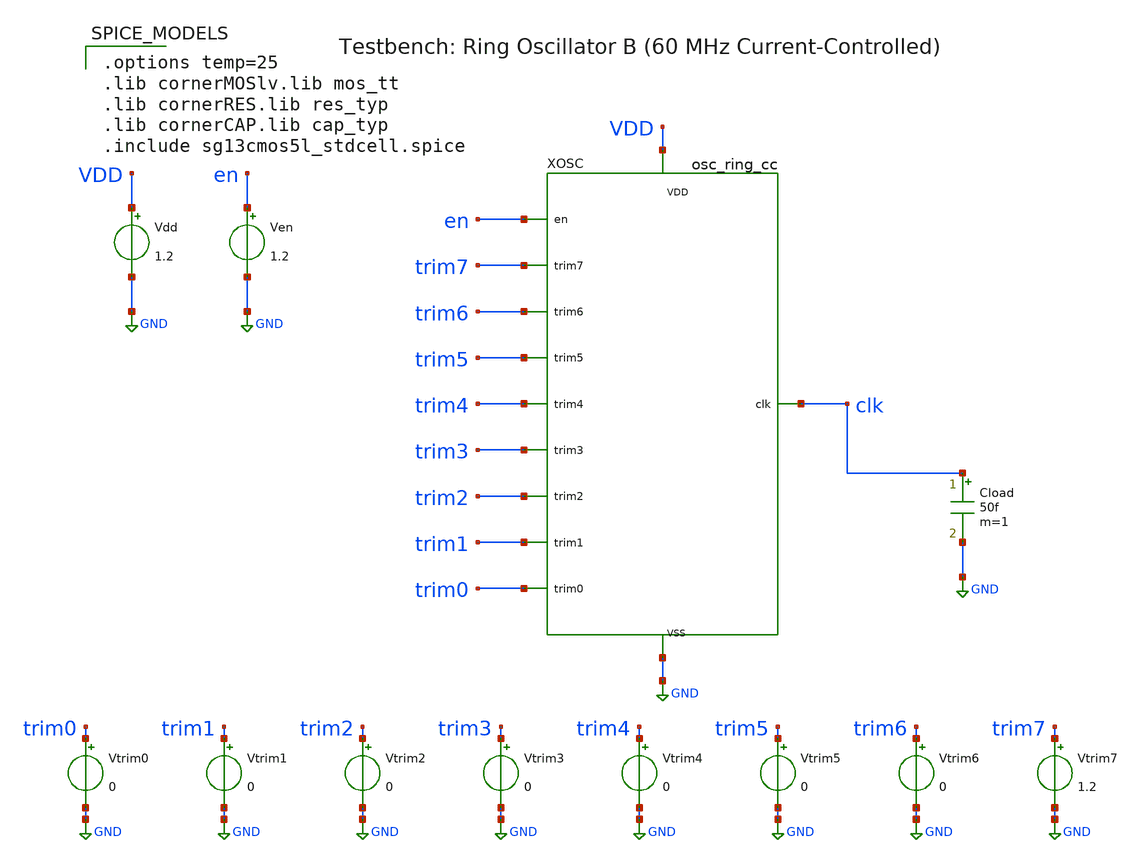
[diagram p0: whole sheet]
** sch_path: analog/osc_ring_cc/tb_osc_ring_cc.sch
**.subckt tb_osc_ring_cc
XOSC VDD GND en trim7 trim6 trim5 trim4 trim3 trim2 trim1 trim0 clk osc_ring_cc
Vdd VDD GND 1.2
Ven en GND 1.2
Vtrim0 trim0 GND 0
Vtrim1 trim1 GND 0
Vtrim2 trim2 GND 0
Vtrim3 trim3 GND 0
Vtrim4 trim4 GND 0
Vtrim5 trim5 GND 0
Vtrim6 trim6 GND 0
Vtrim7 trim7 GND 1.2
Cload clk GND 50f m=1
**** begin user architecture code

.options temp=25
.lib cornerMOSlv.lib mos_tt
.lib cornerRES.lib res_typ
.lib cornerCAP.lib cap_typ
.include sg13cmos5l_stdcell.spice


**** end user architecture code
**.ends

* expanding   symbol:  osc_ring_cc/osc_ring_cc.sym # of pins=12
** sym_path: analog/osc_ring_cc/osc_ring_cc.sym
** sch_path: analog/osc_ring_cc/osc_ring_cc.sch
.subckt osc_ring_cc VDD VSS en trim7 trim6 trim5 trim4 trim3 trim2 trim1 trim0 clk
*.iopin VDD
*.iopin VSS
*.ipin en
*.ipin trim7
*.ipin trim6
*.ipin trim5
*.ipin trim4
*.ipin trim3
*.ipin trim2
*.ipin trim1
*.ipin trim0
*.opin clk
XBIAS VDD VSS en net1 vnbias net2 bias
XIDAC VDD VSS en vnbias trim7 trim6 trim5 trim4 trim3 trim2 trim1 trim0 ictrl idac_8b
XCCO VDD VSS en ictrl clk cco_core
* noconn #net1
* noconn #net2
.ends


* expanding   symbol:  bias/bias.sym # of pins=6
** sym_path: analog/bias/bias.sym
** sch_path: analog/bias/bias.sch
.subckt bias VDD VSS en vpbias vnbias ibias_out
*.iopin VDD
*.iopin VSS
*.ipin en
*.opin vpbias
*.opin vnbias
*.opin ibias_out
XMEN_P enb en VDD VDD sg13_lv_pmos w=0.5u l=0.5u ng=1 m=1 mm_ok=1
XMEN_N enb en VSS VSS sg13_lv_nmos w=0.25u l=0.5u ng=1 m=1 mm_ok=1
XMSU_EN net1 enb VDD VDD sg13_lv_pmos w=0.3u l=1.0u ng=1 m=1 mm_ok=1
XMSU_P1 net2 VSS net1 VDD sg13_lv_pmos w=0.15u l=10u ng=1 m=1 mm_ok=1
XMSU_P2 net3 VSS net2 VDD sg13_lv_pmos w=0.15u l=10u ng=1 m=1 mm_ok=1
XMSU_N net3 vnbias VSS VSS sg13_lv_nmos w=4.0u l=0.5u ng=1 m=1 mm_ok=1
XMSU_INJ vpbias net3 VSS VSS sg13_lv_nmos w=0.5u l=1.0u ng=1 m=1 mm_ok=1
XMP1 vnbias vpbias VDD VDD sg13_lv_pmos w=1.0u l=4.0u ng=1 m=1 mm_ok=1
XMN1 vnbias vnbias VSS VSS sg13_lv_nmos w=0.3u l=4.0u ng=1 m=1 mm_ok=1
XMP2 vpbias vpbias VDD VDD sg13_lv_pmos w=1.0u l=4.0u ng=1 m=1 mm_ok=1
XMN2 vpbias vnbias net4 VSS sg13_lv_nmos w=0.3u l=4.0u ng=1 m=4 mm_ok=1
XR_BIAS net4 VSS VSS rppd w=0.5e-6 l=20.0e-6 m=1 b=19 mm_ok=1
XMP_OFF vpbias en VDD VDD sg13_lv_pmos w=1.0u l=0.5u ng=1 m=1 mm_ok=1
XMN_OFF vnbias enb VSS VSS sg13_lv_nmos w=1.0u l=0.5u ng=1 m=1 mm_ok=1
XMP_OUT ibias_out vpbias VDD VDD sg13_lv_pmos w=1.0u l=4.0u ng=1 m=1 mm_ok=1
.ends


* expanding   symbol:  osc_ring_cc/idac_8b.sym # of pins=13
** sym_path: analog/osc_ring_cc/idac_8b.sym
** sch_path: analog/osc_ring_cc/idac_8b.sch
.subckt idac_8b VDD VSS en vnbias trim7 trim6 trim5 trim4 trim3 trim2 trim1 trim0 ictrl
*.iopin VDD
*.iopin VSS
*.ipin en
*.ipin vnbias
*.ipin trim7
*.ipin trim6
*.ipin trim5
*.ipin trim4
*.ipin trim3
*.ipin trim2
*.ipin trim1
*.ipin trim0
*.opin ictrl
XMN_DIV vpdac vnbias VSS VSS sg13_lv_nmos w=0.3u l=4.0u ng=1 m=1 mm_ok=1
XMP_IN vpdac vpdac VDD VDD sg13_lv_pmos w=1.5u l=4.0u ng=1 m=2 mm_ok=1
XMP_DAC_OFF vpdac en VDD VDD sg13_lv_pmos w=0.5u l=0.5u ng=1 m=1 mm_ok=1
XINV_EN enb en VDD VSS sg13cmos5l_inv_1
XINV_B0 b0_b trim0 VDD VSS sg13cmos5l_inv_1
XINV_B1 b1_b trim1 VDD VSS sg13cmos5l_inv_1
XINV_B2 b2_b trim2 VDD VSS sg13cmos5l_inv_1
XINV_B3 b3_b trim3 VDD VSS sg13cmos5l_inv_1
XINV_B4 b4_b trim4 VDD VSS sg13cmos5l_inv_1
XINV_A t3_b trim7 VDD VSS sg13cmos5l_inv_1
XN_AB t5_b trim7 trim6 VDD VSS sg13cmos5l_nand2_2
XI_AB ab t5_b VDD VSS sg13cmos5l_inv_1
XN_ABC t6_b ab trim5 VDD VSS sg13cmos5l_nand2_2
XN_BC bc_n trim6 trim5 VDD VSS sg13cmos5l_nand2_2
XI_BC bc bc_n VDD VSS sg13cmos5l_inv_1
XNO_T2 t2_b trim7 bc VDD VSS sg13cmos5l_nor2_1
XNO_BORC borc_n trim6 trim5 VDD VSS sg13cmos5l_nor2_1
XI_BORC borc borc_n VDD VSS sg13cmos5l_inv_1
XN_T4 t4_b trim7 borc VDD VSS sg13cmos5l_nand2_2
XNO_T1 t1_b trim7 trim6 VDD VSS sg13cmos5l_nor2_1
XNO_T0 t0_b trim7 borc VDD VSS sg13cmos5l_nor2_1
XMPC_PED net1 vpdac VDD VDD sg13_lv_pmos w=0.5u l=4.0u ng=1 m=48 mm_ok=1
XMPS_PED ictrl enb net1 VDD sg13_lv_pmos w=1.0u l=0.2u ng=1 m=4 mm_ok=1
XMPC_B0 net2 vpdac VDD VDD sg13_lv_pmos w=0.5u l=4.0u ng=1 m=1 mm_ok=1
XMPS_B0 ictrl b0_b net2 VDD sg13_lv_pmos w=1.0u l=0.2u ng=1 m=1 mm_ok=1
XMPC_B1 net3 vpdac VDD VDD sg13_lv_pmos w=0.5u l=4.0u ng=1 m=2 mm_ok=1
XMPS_B1 ictrl b1_b net3 VDD sg13_lv_pmos w=1.0u l=0.2u ng=1 m=1 mm_ok=1
XMPC_B2 net4 vpdac VDD VDD sg13_lv_pmos w=0.5u l=4.0u ng=1 m=4 mm_ok=1
XMPS_B2 ictrl b2_b net4 VDD sg13_lv_pmos w=1.0u l=0.2u ng=1 m=1 mm_ok=1
XMPC_B3 net5 vpdac VDD VDD sg13_lv_pmos w=0.5u l=4.0u ng=1 m=8 mm_ok=1
XMPS_B3 ictrl b3_b net5 VDD sg13_lv_pmos w=1.0u l=0.2u ng=1 m=1 mm_ok=1
XMPC_B4 net6 vpdac VDD VDD sg13_lv_pmos w=0.5u l=4.0u ng=1 m=16 mm_ok=1
XMPS_B4 ictrl b4_b net6 VDD sg13_lv_pmos w=1.0u l=0.2u ng=1 m=2 mm_ok=1
XMPC_T0 net7 vpdac VDD VDD sg13_lv_pmos w=0.5u l=4.0u ng=1 m=32 mm_ok=1
XMPS_T0 ictrl t0_b net7 VDD sg13_lv_pmos w=1.0u l=0.2u ng=1 m=4 mm_ok=1
XMPC_T1 net8 vpdac VDD VDD sg13_lv_pmos w=0.5u l=4.0u ng=1 m=32 mm_ok=1
XMPS_T1 ictrl t1_b net8 VDD sg13_lv_pmos w=1.0u l=0.2u ng=1 m=4 mm_ok=1
XMPC_T2 net9 vpdac VDD VDD sg13_lv_pmos w=0.5u l=4.0u ng=1 m=32 mm_ok=1
XMPS_T2 ictrl t2_b net9 VDD sg13_lv_pmos w=1.0u l=0.2u ng=1 m=4 mm_ok=1
XMPC_T3 net10 vpdac VDD VDD sg13_lv_pmos w=0.5u l=4.0u ng=1 m=32 mm_ok=1
XMPS_T3 ictrl t3_b net10 VDD sg13_lv_pmos w=1.0u l=0.2u ng=1 m=4 mm_ok=1
XMPC_T4 net11 vpdac VDD VDD sg13_lv_pmos w=0.5u l=4.0u ng=1 m=32 mm_ok=1
XMPS_T4 ictrl t4_b net11 VDD sg13_lv_pmos w=1.0u l=0.2u ng=1 m=4 mm_ok=1
XMPC_T5 net12 vpdac VDD VDD sg13_lv_pmos w=0.5u l=4.0u ng=1 m=32 mm_ok=1
XMPS_T5 ictrl t5_b net12 VDD sg13_lv_pmos w=1.0u l=0.2u ng=1 m=4 mm_ok=1
XMPC_T6 net13 vpdac VDD VDD sg13_lv_pmos w=0.5u l=4.0u ng=1 m=32 mm_ok=1
XMPS_T6 ictrl t6_b net13 VDD sg13_lv_pmos w=1.0u l=0.2u ng=1 m=4 mm_ok=1
.ends


* expanding   symbol:  osc_ring_cc/cco_core.sym # of pins=5
** sym_path: analog/osc_ring_cc/cco_core.sym
** sch_path: analog/osc_ring_cc/cco_core.sch
.subckt cco_core VDD VSS en ictrl clk
*.iopin VDD
*.iopin VSS
*.ipin en
*.ipin ictrl
*.opin clk
XINV_EN enb en VDD VSS sg13cmos5l_inv_1
XMN_BIAS ictrl ictrl VSS VSS sg13_lv_nmos w=2.0u l=1.0u ng=1 m=2 mm_ok=1
XMP_BIAS vctrl_p vctrl_p VDD VDD sg13_lv_pmos w=4.0u l=1.0u ng=1 m=2 mm_ok=1
XMN_BMIR vctrl_p ictrl VSS VSS sg13_lv_nmos w=2.0u l=1.0u ng=1 m=2 mm_ok=1
XMP_POFF vctrl_p en VDD VDD sg13_lv_pmos w=0.5u l=0.5u ng=1 m=1 mm_ok=1
XMN_NOFF ictrl enb VSS VSS sg13_lv_nmos w=0.5u l=0.5u ng=1 m=1 mm_ok=1
XMPC_0 net1 vctrl_p VDD VDD sg13_lv_pmos w=4.0u l=1.0u ng=1 m=1 mm_ok=1
XMPI_0 n1 n0 net1 VDD sg13_lv_pmos w=1.0u l=0.2u ng=1 m=1 mm_ok=1
XMNI_0 n1 n0 net2 VSS sg13_lv_nmos w=0.5u l=0.2u ng=1 m=1 mm_ok=1
XMNC_0 net2 ictrl VSS VSS sg13_lv_nmos w=2.0u l=1.0u ng=1 m=1 mm_ok=1
XCC_0 n1 VSS cap_cmomf w=2.4e-6 l=2.4e-6 mmin=1 mmax=4 subblock=0 rfmodel=0 subscale=1 m=1 mm_ok=1
XMPC_1 net3 vctrl_p VDD VDD sg13_lv_pmos w=4.0u l=1.0u ng=1 m=1 mm_ok=1
XMPI_1 n2 n1 net3 VDD sg13_lv_pmos w=1.0u l=0.2u ng=1 m=1 mm_ok=1
XMNI_1 n2 n1 net4 VSS sg13_lv_nmos w=0.5u l=0.2u ng=1 m=1 mm_ok=1
XMNC_1 net4 ictrl VSS VSS sg13_lv_nmos w=2.0u l=1.0u ng=1 m=1 mm_ok=1
XCC_1 n2 VSS cap_cmomf w=2.4e-6 l=2.4e-6 mmin=1 mmax=4 subblock=0 rfmodel=0 subscale=1 m=1 mm_ok=1
XMPC_2 net5 vctrl_p VDD VDD sg13_lv_pmos w=4.0u l=1.0u ng=1 m=1 mm_ok=1
XMPI_2 n3 n2 net5 VDD sg13_lv_pmos w=1.0u l=0.2u ng=1 m=1 mm_ok=1
XMNI_2 n3 n2 net6 VSS sg13_lv_nmos w=0.5u l=0.2u ng=1 m=1 mm_ok=1
XMNC_2 net6 ictrl VSS VSS sg13_lv_nmos w=2.0u l=1.0u ng=1 m=1 mm_ok=1
XCC_2 n3 VSS cap_cmomf w=2.4e-6 l=2.4e-6 mmin=1 mmax=4 subblock=0 rfmodel=0 subscale=1 m=1 mm_ok=1
XMPC_3 net7 vctrl_p VDD VDD sg13_lv_pmos w=4.0u l=1.0u ng=1 m=1 mm_ok=1
XMPI_3 n4 n3 net7 VDD sg13_lv_pmos w=1.0u l=0.2u ng=1 m=1 mm_ok=1
XMNI_3 n4 n3 net8 VSS sg13_lv_nmos w=0.5u l=0.2u ng=1 m=1 mm_ok=1
XMNC_3 net8 ictrl VSS VSS sg13_lv_nmos w=2.0u l=1.0u ng=1 m=1 mm_ok=1
XCC_3 n4 VSS cap_cmomf w=2.4e-6 l=2.4e-6 mmin=1 mmax=4 subblock=0 rfmodel=0 subscale=1 m=1 mm_ok=1
XMPC_4 net9 vctrl_p VDD VDD sg13_lv_pmos w=4.0u l=1.0u ng=1 m=1 mm_ok=1
XMPI_4 n0 n4 net9 VDD sg13_lv_pmos w=1.0u l=0.2u ng=1 m=1 mm_ok=1
XMNI_4 n0 n4 net10 VSS sg13_lv_nmos w=0.5u l=0.2u ng=1 m=1 mm_ok=1
XMNC_4 net10 ictrl VSS VSS sg13_lv_nmos w=2.0u l=1.0u ng=1 m=1 mm_ok=1
XCC_4 n0 VSS cap_cmomf w=2.4e-6 l=2.4e-6 mmin=1 mmax=4 subblock=0 rfmodel=0 subscale=1 m=1 mm_ok=1
XMN_RST n4 enb VSS VSS sg13_lv_nmos w=0.5u l=0.5u ng=1 m=1 mm_ok=1
XBUF1 net11 n4 VDD VSS sg13cmos5l_inv_1
XBUF2 net12 net11 VDD VSS sg13cmos5l_inv_2
XBUF4 clk net12 VDD VSS sg13cmos5l_buf_4
.ends

.GLOBAL GND
.end
